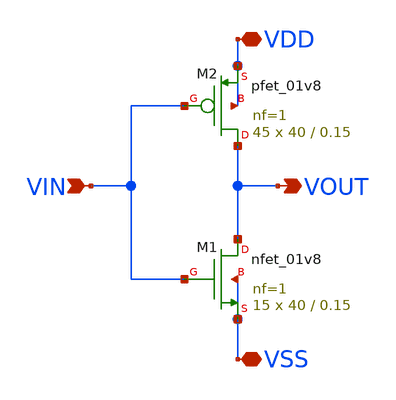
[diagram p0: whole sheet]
** sch_path: xschem/DC_DC_Converter_xschem/OTHERS/DC_DC_Converter_JV11/Inverter_3/Inverter3.sch
**.subckt Inverter3 VIN VDD VSS VOUT
*.ipin VIN
*.iopin VDD
*.iopin VSS
*.opin VOUT
XM1 VOUT VIN VSS VSS sky130_fd_pr__nfet_01v8 L=0.15 W=40 nf=1 ad='int((nf+1)/2) * W/nf * 0.29' as='int((nf+2)/2) * W/nf * 0.29'
+ pd='2*int((nf+1)/2) * (W/nf + 0.29)' ps='2*int((nf+2)/2) * (W/nf + 0.29)' nrd='0.29 / W' nrs='0.29 / W'
+ sa=0 sb=0 sd=0 mult=15 m=15
XM2 VOUT VIN VDD VDD sky130_fd_pr__pfet_01v8 L=0.15 W=40 nf=1 ad='int((nf+1)/2) * W/nf * 0.29' as='int((nf+2)/2) * W/nf * 0.29'
+ pd='2*int((nf+1)/2) * (W/nf + 0.29)' ps='2*int((nf+2)/2) * (W/nf + 0.29)' nrd='0.29 / W' nrs='0.29 / W'
+ sa=0 sb=0 sd=0 mult=45 m=45
**.ends
.end
